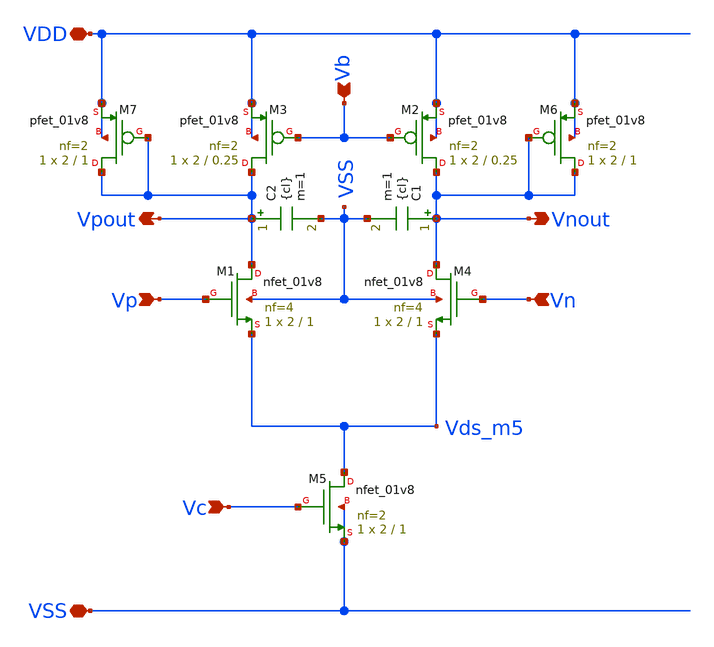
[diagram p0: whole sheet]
** sch_path: custom_gds/tt_um_georgboecherer_vco/xschem/vco_stage_2.sch
**.subckt vco_stage_2 VDD VSS Vp Vn Vb Vc Vpout Vnout
*.iopin VDD
*.iopin VSS
*.ipin Vp
*.ipin Vn
*.ipin Vb
*.ipin Vc
*.opin Vpout
*.opin Vnout
XM1 Vpout Vp Vds_m5 VSS sky130_fd_pr__nfet_01v8 L=1 W=2 nf=4 ad='int((nf+1)/2) * W/nf * 0.29' as='int((nf+2)/2) * W/nf * 0.29'
+ pd='2*int((nf+1)/2) * (W/nf + 0.29)' ps='2*int((nf+2)/2) * (W/nf + 0.29)' nrd='0.29 / W' nrs='0.29 / W'
+ sa=0 sb=0 sd=0 mult=1 m=1
XM4 Vnout Vn Vds_m5 VSS sky130_fd_pr__nfet_01v8 L=1 W=2 nf=4 ad='int((nf+1)/2) * W/nf * 0.29' as='int((nf+2)/2) * W/nf * 0.29'
+ pd='2*int((nf+1)/2) * (W/nf + 0.29)' ps='2*int((nf+2)/2) * (W/nf + 0.29)' nrd='0.29 / W' nrs='0.29 / W'
+ sa=0 sb=0 sd=0 mult=1 m=1
XM5 Vds_m5 Vc VSS VSS sky130_fd_pr__nfet_01v8 L=1 W=2 nf=2 ad='int((nf+1)/2) * W/nf * 0.29' as='int((nf+2)/2) * W/nf * 0.29'
+ pd='2*int((nf+1)/2) * (W/nf + 0.29)' ps='2*int((nf+2)/2) * (W/nf + 0.29)' nrd='0.29 / W' nrs='0.29 / W'
+ sa=0 sb=0 sd=0 mult=1 m=1
XM2 Vnout Vb VDD VDD sky130_fd_pr__pfet_01v8 L=0.25 W=2 nf=2 ad='int((nf+1)/2) * W/nf * 0.29' as='int((nf+2)/2) * W/nf * 0.29'
+ pd='2*int((nf+1)/2) * (W/nf + 0.29)' ps='2*int((nf+2)/2) * (W/nf + 0.29)' nrd='0.29 / W' nrs='0.29 / W'
+ sa=0 sb=0 sd=0 mult=1 m=1
XM3 Vpout Vb VDD VDD sky130_fd_pr__pfet_01v8 L=0.25 W=2 nf=2 ad='int((nf+1)/2) * W/nf * 0.29' as='int((nf+2)/2) * W/nf * 0.29'
+ pd='2*int((nf+1)/2) * (W/nf + 0.29)' ps='2*int((nf+2)/2) * (W/nf + 0.29)' nrd='0.29 / W' nrs='0.29 / W'
+ sa=0 sb=0 sd=0 mult=1 m=1
C1 Vnout VSS {cl} m=1
C2 Vpout VSS {cl} m=1
XM6 Vnout Vnout VDD VDD sky130_fd_pr__pfet_01v8 L=1 W=2 nf=2 ad='int((nf+1)/2) * W/nf * 0.29' as='int((nf+2)/2) * W/nf * 0.29'
+ pd='2*int((nf+1)/2) * (W/nf + 0.29)' ps='2*int((nf+2)/2) * (W/nf + 0.29)' nrd='0.29 / W' nrs='0.29 / W'
+ sa=0 sb=0 sd=0 mult=1 m=1
XM7 Vpout Vpout VDD VDD sky130_fd_pr__pfet_01v8 L=1 W=2 nf=2 ad='int((nf+1)/2) * W/nf * 0.29' as='int((nf+2)/2) * W/nf * 0.29'
+ pd='2*int((nf+1)/2) * (W/nf + 0.29)' ps='2*int((nf+2)/2) * (W/nf + 0.29)' nrd='0.29 / W' nrs='0.29 / W'
+ sa=0 sb=0 sd=0 mult=1 m=1
**.ends
.end
